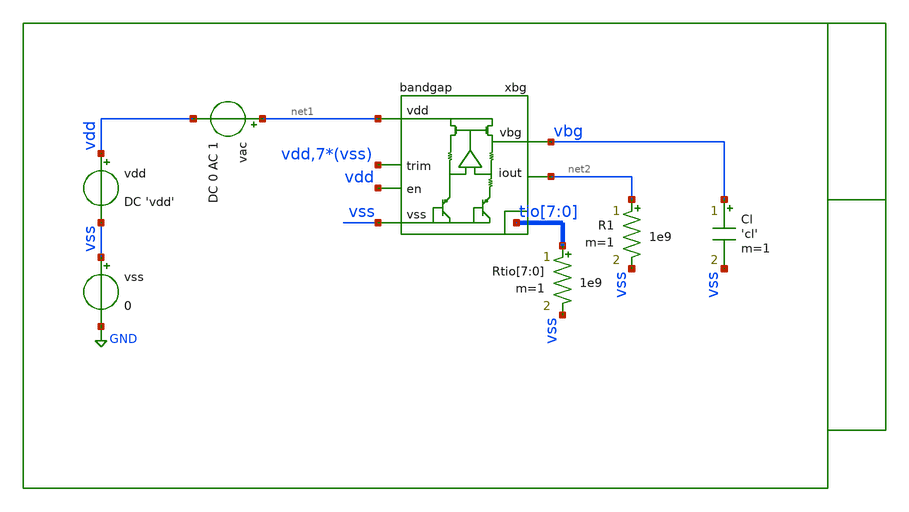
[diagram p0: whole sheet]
** sch_path: xschem/tb/bandgap_cm/bandgap/ac_bandgap_psrr.sch
**.subckt ac_bandgap_psrr
vdd vdd vss DC 'vdd'
vss vss GND 0
vac net1 vdd DC 0 AC 1
Cl vbg vss 'cl' m=1
xbg net1 vbg vss tio[7] tio[6] tio[5] tio[4] tio[3] tio[2] tio[1] tio[0] vdd vss vss vss vss vss vss
+ vss net2 vdd bandgap
R1 net2 vss 1e9 m=1
Rtio[7] tio[7] vss 1e9 m=1
Rtio[6] tio[6] vss 1e9 m=1
Rtio[5] tio[5] vss 1e9 m=1
Rtio[4] tio[4] vss 1e9 m=1
Rtio[3] tio[3] vss 1e9 m=1
Rtio[2] tio[2] vss 1e9 m=1
Rtio[1] tio[1] vss 1e9 m=1
Rtio[0] tio[0] vss 1e9 m=1
**** begin user architecture code

* Control

.param vdd = 3.3
.param cl = 100e-15

.temp 27

.options reltol = 1e-6

*------------------------------------------------------------
* Nodeset for better convergence
*------------------------------------------------------------
.nodeset v(vbg)  = '1'
.nodeset v(xbg.gate) = 'vdd/2'
.nodeset v(xbg.vx)   = '0.70'
.nodeset v(xbg.vbe2) = '0.65'
.nodeset v(xbg.vs1)  = '0'
*------------------------------------------------------------

.control

save all
ac dec 10 0.01 1e9

let psrr=(1/vbg)
let psrr_db = vdb(psrr)
gnuplot p1 psrr_db

meas ac psrr_dc find psrr_db at=0.01
meas ac psrr_1hz find psrr_db at=1
meas ac psrr_1khz find psrr_db at=1e3
meas ac psrr_10khz find psrr_db at=10e3
meas ac psrr_100khz find psrr_db at=100e3

print psrr_dc
print psrr_1hz
print psrr_1khz
print psrr_10khz
print psrr_100khz

set wr_singlescale
set wr_vecnames
wrdata data.csv psrr psrr_db

.endc
.end


 * Model Corners

.include $::CORNERS/ngspice/tt.spice
*.include $::CORNERS/ngspice/ff.spice
*.include $::CORNERS/ngspice/ss.spice
*.include $::CORNERS/ngspice/sf.spice
*.include $::CORNERS/ngspice/fs.spice

**** end user architecture code
**.ends
.GLOBAL GND
.end
